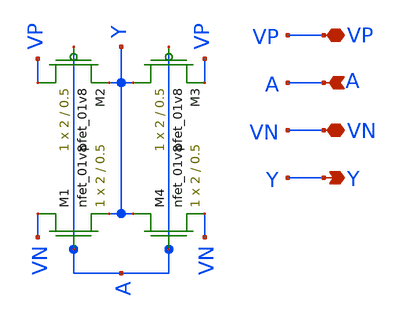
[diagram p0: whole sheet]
** sch_path: LDS/LDS_inverter.sch
**.subckt LDS_inverter VP A Y VN
*.iopin VP
*.ipin A
*.opin Y
*.iopin VN
XM3 Y A VP VP sky130_fd_pr__pfet_01v8 L=0.5 W=2 nf=1 ad='int((nf+1)/2) * W/nf * 0.29' as='int((nf+2)/2) * W/nf * 0.29'
+ pd='2*int((nf+1)/2) * (W/nf + 0.29)' ps='2*int((nf+2)/2) * (W/nf + 0.29)' nrd='0.29 / W' nrs='0.29 / W'
+ sa=0 sb=0 sd=0 mult=1 m=1
XM4 Y A VN VN sky130_fd_pr__nfet_01v8 L=0.5 W=2 nf=1 ad='int((nf+1)/2) * W/nf * 0.29' as='int((nf+2)/2) * W/nf * 0.29'
+ pd='2*int((nf+1)/2) * (W/nf + 0.29)' ps='2*int((nf+2)/2) * (W/nf + 0.29)' nrd='0.29 / W' nrs='0.29 / W'
+ sa=0 sb=0 sd=0 mult=1 m=1
XM1 VN A Y VN sky130_fd_pr__nfet_01v8 L=0.5 W=2 nf=1 ad='int((nf+1)/2) * W/nf * 0.29' as='int((nf+2)/2) * W/nf * 0.29'
+ pd='2*int((nf+1)/2) * (W/nf + 0.29)' ps='2*int((nf+2)/2) * (W/nf + 0.29)' nrd='0.29 / W' nrs='0.29 / W'
+ sa=0 sb=0 sd=0 mult=1 m=1
XM2 VP A Y VP sky130_fd_pr__pfet_01v8 L=0.5 W=2 nf=1 ad='int((nf+1)/2) * W/nf * 0.29' as='int((nf+2)/2) * W/nf * 0.29'
+ pd='2*int((nf+1)/2) * (W/nf + 0.29)' ps='2*int((nf+2)/2) * (W/nf + 0.29)' nrd='0.29 / W' nrs='0.29 / W'
+ sa=0 sb=0 sd=0 mult=1 m=1
**.ends
.end
